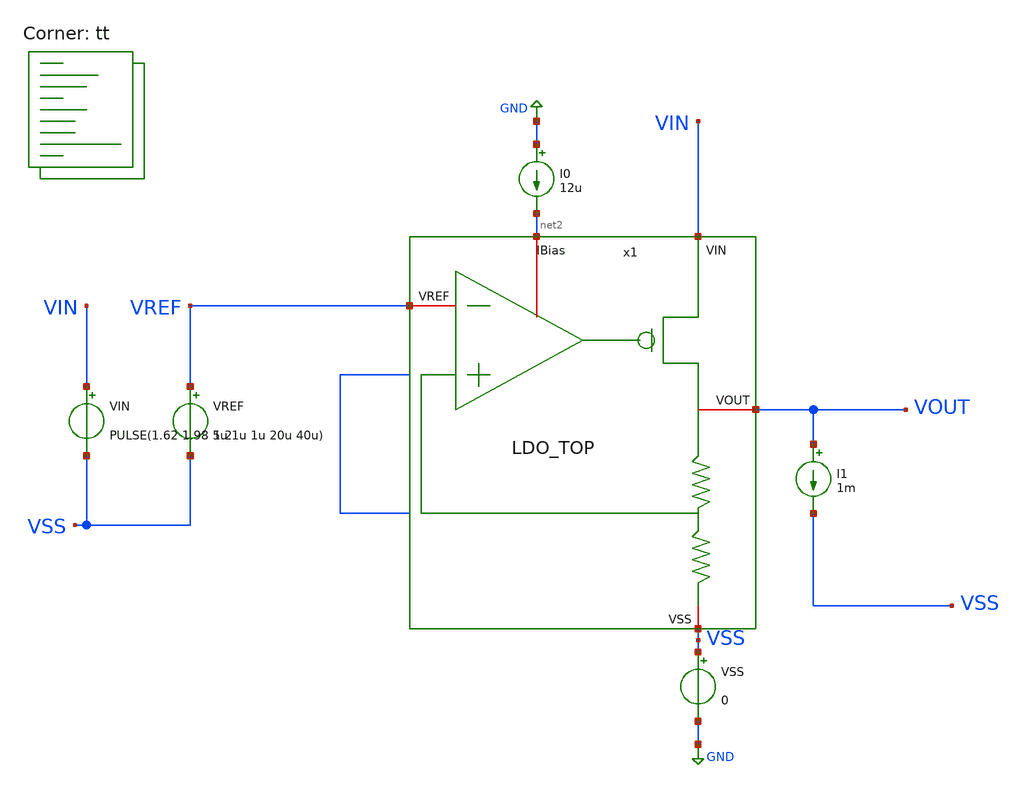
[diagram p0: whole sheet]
** sch_path: LDO_1p5V/tests/Line_tran.sch
**.subckt Line_tran
VSS VSS GND 0
VREF VREF VSS 1.2
VIN VIN VSS PULSE(1.62 1.98 5u 1u 1u 20u 40u)
I0 GND net2 12u
I1 VOUT VSS 1m
x1 VIN net2 VREF VOUT VSS LDO_TOP
**** begin user architecture code


.options savecurrents
.save all
.save v(x1.vgate)

.control
set filetype=ascii

echo ==========================================
echo ===== LDO LINE TRANSIENT ANALYSIS =====
echo ==========================================

op

echo ===== OPERATING POINT =====
print v(VIN)
print v(VOUT)
print v(VREF)
print v(x1.vgate)

echo ===== TRANSIENT ANALYSIS =====

* Fuente VIN recomendada en el esquemático:
* VIN PULSE(1.62 1.98 5u 1u 1u 20u 40u)
*
* Carga fija recomendada:
* ILOAD1 DC 1m

tran 10n 100u

echo ==========================================
echo ===== LINE TRANSIENT MEASUREMENTS =====
echo ==========================================

* VOUT nominal = 1.5 V
* Settling band = +/-1%
* Lower band = 1.485 V
* Upper band = 1.515 V

****************************************************
* GLOBAL MIN/MAX
****************************************************

meas tran vout_min_all min v(VOUT)
meas tran vout_max_all max v(VOUT)

let global_undershoot_mv = (1.5 - vout_min_all)*1000
let global_overshoot_mv  = (vout_max_all - 1.5)*1000

****************************************************
* STEP 1: VIN RISE 1.62V -> 1.98V
* Starts at 5us, ends at 6us
****************************************************

meas tran vout_max_step1 max v(VOUT) from=5u to=26u
meas tran vout_min_step1 min v(VOUT) from=5u to=26u

let overshoot_step1_mv  = (vout_max_step1 - 1.5)*1000
let undershoot_step1_mv = (1.5 - vout_min_step1)*1000

* Settling after VIN rise:
* If VOUT goes above nominal, measure when it returns below upper band.
meas tran t_settle_step1_abs when v(VOUT)=1.515 fall=1 from=5u to=26u

let t_settle_step1 = t_settle_step1_abs - 5u
let t_settle_step1_us = t_settle_step1*1e6

****************************************************
* STEP 2: VIN FALL 1.98V -> 1.62V
* Starts at 26us, ends at 27us
****************************************************

meas tran vout_max_step2 max v(VOUT) from=26u to=45u
meas tran vout_min_step2 min v(VOUT) from=26u to=45u

let overshoot_step2_mv  = (vout_max_step2 - 1.5)*1000
let undershoot_step2_mv = (1.5 - vout_min_step2)*1000

* Settling after VIN fall:
* If VOUT goes below nominal, measure when it returns above lower band.
meas tran t_settle_step2_abs when v(VOUT)=1.485 rise=1 from=26u to=45u

let t_settle_step2 = t_settle_step2_abs - 26u
let t_settle_step2_us = t_settle_step2*1e6

****************************************************
* STEP 3: SECOND VIN RISE 1.62V -> 1.98V
* Starts at 45us, ends at 46us
****************************************************

meas tran vout_max_step3 max v(VOUT) from=45u to=66u
meas tran vout_min_step3 min v(VOUT) from=45u to=66u

let overshoot_step3_mv  = (vout_max_step3 - 1.5)*1000
let undershoot_step3_mv = (1.5 - vout_min_step3)*1000

meas tran t_settle_step3_abs when v(VOUT)=1.515 fall=1 from=45u to=66u

let t_settle_step3 = t_settle_step3_abs - 45u
let t_settle_step3_us = t_settle_step3*1e6

****************************************************
* STEP 4: SECOND VIN FALL 1.98V -> 1.62V
* Starts at 66us, ends at 67us
****************************************************

meas tran vout_max_step4 max v(VOUT) from=66u to=85u
meas tran vout_min_step4 min v(VOUT) from=66u to=85u

let overshoot_step4_mv  = (vout_max_step4 - 1.5)*1000
let undershoot_step4_mv = (1.5 - vout_min_step4)*1000

meas tran t_settle_step4_abs when v(VOUT)=1.485 rise=1 from=66u to=85u

let t_settle_step4 = t_settle_step4_abs - 66u
let t_settle_step4_us = t_settle_step4*1e6

****************************************************
* RESULTS
****************************************************

echo ===== GLOBAL RESULTS =====
print vout_min_all
print vout_max_all
print global_undershoot_mv
print global_overshoot_mv

echo ===== STEP 1: VIN 1.62V -> 1.98V =====
print vout_max_step1
print vout_min_step1
print overshoot_step1_mv
print undershoot_step1_mv
print t_settle_step1_us

echo ===== STEP 2: VIN 1.98V -> 1.62V =====
print vout_max_step2
print vout_min_step2
print overshoot_step2_mv
print undershoot_step2_mv
print t_settle_step2_us

echo ===== STEP 3: VIN 1.62V -> 1.98V =====
print vout_max_step3
print vout_min_step3
print overshoot_step3_mv
print undershoot_step3_mv
print t_settle_step3_us

echo ===== STEP 4: VIN 1.98V -> 1.62V =====
print vout_max_step4
print vout_min_step4
print overshoot_step4_mv
print undershoot_step4_mv
print t_settle_step4_us

****************************************************
* PLOTS
****************************************************

echo ===== PLOTS =====

plot v(VIN)
plot v(VOUT)
plot v(x1.vgate)
plot v(VOUT) v(VIN)
plot v(VOUT) v(x1.vgate)

.endc


.lib $::SKYWATER_MODELS/sky130.lib.spice tt
**** end user architecture code
**.ends

* expanding   symbol:  /foss/designs/Curso_Semiconductores/LDO_1p5V/schematics/LDO_TOP.sym # of
*+ pins=5
** sym_path: LDO/LDO_TOP.sym
** sch_path: LDO/LDO_TOP.sch
.subckt LDO_TOP VIN IBias VREF VOUT VSS
*.iopin VIN
*.iopin VREF
*.iopin IBias
*.iopin VOUT
*.iopin VSS
x1 VIN IBias VREF VOUT net1 net1 VSS LDO
.ends


* expanding   symbol:  /foss/designs/Curso_Semiconductores/LDO/LDO.sym # of pins=7
** sym_path: LDO/LDO.sym
** sch_path: LDO/LDO.sch
.subckt LDO VIN IBias VREF VOUT VFB1 VFB2 VSS
*.iopin VIN
*.iopin VREF
*.iopin VFB1
*.iopin VSS
*.iopin VFB2
*.iopin VOUT
*.iopin IBias
XM7 VOUT Vgate VIN VIN sky130_fd_pr__pfet_01v8 L=0.15 W=6 nf=1 ad='int((1 + 1)/2) * 6 / 1 * 0.29' as='int((1 + 2)/2) * 6 / 1 * 0.29'
+ pd='2*int((1 + 1)/2) * (6 / 1 + 0.29)' ps='2*int((1 + 2)/2) * (6 / 1 + 0.29)' nrd='0.29 / 6 ' nrs='0.29 / 6 '
+ sa=0 sb=0 sd=0 mult=50 m=50
XC3 Vgate VOUT sky130_fd_pr__model__cap_mim W=10 L=10 MF=1 m=1
x1 VIN Vgate VREF VFB1 IBias VSS OTA_5T
x2 VOUT VFB2 VSS RES_FB
.ends


* expanding   symbol:  /foss/designs/Curso_Semiconductores/OTA_5T/OTA_5T.sym # of pins=6
** sym_path: /foss/designs/Curso_Semiconductores/OTA_5T/OTA_5T.sym
** sch_path: /foss/designs/Curso_Semiconductores/OTA_5T/OTA_5T.sch
.subckt OTA_5T VIN VOUT_AMP VINN VINP IB VSS
*.iopin VIN
*.iopin VSS
*.iopin VOUT_AMP
*.iopin IB
*.iopin VINN
*.iopin VINP
XM1 IB IB VSS VSS sky130_fd_pr__nfet_01v8 L=1 W=2.5 nf=1 ad='int((1 + 1)/2) * 2.5 / 1 * 0.29' as='int((1 + 2)/2) * 2.5 / 1 * 0.29'
+ pd='2*int((1 + 1)/2) * (2.5 / 1 + 0.29)' ps='2*int((1 + 2)/2) * (2.5 / 1 + 0.29)' nrd='0.29 / 2.5 ' nrs='0.29 / 2.5 '
+ sa=0 sb=0 sd=0 mult=4 m=4
XM2 tail IB VSS VSS sky130_fd_pr__nfet_01v8 L=1 W=2.5 nf=1 ad='int((1 + 1)/2) * 2.5 / 1 * 0.29' as='int((1 + 2)/2) * 2.5 / 1 * 0.29'
+ pd='2*int((1 + 1)/2) * (2.5 / 1 + 0.29)' ps='2*int((1 + 2)/2) * (2.5 / 1 + 0.29)' nrd='0.29 / 2.5 ' nrs='0.29 / 2.5 '
+ sa=0 sb=0 sd=0 mult=4 m=4
XM3 net1 VINP tail VSS sky130_fd_pr__nfet_01v8 L=1 W=3 nf=1 ad='int((1 + 1)/2) * 3 / 1 * 0.29' as='int((1 + 2)/2) * 3 / 1 * 0.29'
+ pd='2*int((1 + 1)/2) * (3 / 1 + 0.29)' ps='2*int((1 + 2)/2) * (3 / 1 + 0.29)' nrd='0.29 / 3 ' nrs='0.29 / 3 '
+ sa=0 sb=0 sd=0 mult=4 m=4
XM4 VOUT_AMP VINN tail VSS sky130_fd_pr__nfet_01v8 L=1 W=3 nf=1 ad='int((1 + 1)/2) * 3 / 1 * 0.29' as='int((1 + 2)/2) * 3 / 1 * 0.29'
+ pd='2*int((1 + 1)/2) * (3 / 1 + 0.29)' ps='2*int((1 + 2)/2) * (3 / 1 + 0.29)' nrd='0.29 / 3 ' nrs='0.29 / 3 '
+ sa=0 sb=0 sd=0 mult=4 m=4
XM5 VOUT_AMP net1 VIN VIN sky130_fd_pr__pfet_01v8 L=1 W=6 nf=1 ad='int((1 + 1)/2) * 6 / 1 * 0.29' as='int((1 + 2)/2) * 6 / 1 * 0.29'
+ pd='2*int((1 + 1)/2) * (6 / 1 + 0.29)' ps='2*int((1 + 2)/2) * (6 / 1 + 0.29)' nrd='0.29 / 6 ' nrs='0.29 / 6 '
+ sa=0 sb=0 sd=0 mult=4 m=4
XM6 net1 net1 VIN VIN sky130_fd_pr__pfet_01v8 L=1 W=6 nf=1 ad='int((1 + 1)/2) * 6 / 1 * 0.29' as='int((1 + 2)/2) * 6 / 1 * 0.29'
+ pd='2*int((1 + 1)/2) * (6 / 1 + 0.29)' ps='2*int((1 + 2)/2) * (6 / 1 + 0.29)' nrd='0.29 / 6 ' nrs='0.29 / 6 '
+ sa=0 sb=0 sd=0 mult=4 m=4
XD tail VSS tail VSS sky130_fd_pr__nfet_01v8 L=0.15 W=3 nf=1 ad='int((1 + 1)/2) * 3 / 1 * 0.29' as='int((1 + 2)/2) * 3 / 1 * 0.29'
+ pd='2*int((1 + 1)/2) * (3 / 1 + 0.29)' ps='2*int((1 + 2)/2) * (3 / 1 + 0.29)' nrd='0.29 / 3 ' nrs='0.29 / 3 '
+ sa=0 sb=0 sd=0 mult=4 m=4
XM7 VIN VIN VIN VIN sky130_fd_pr__pfet_01v8 L=0.15 W=6 nf=1 ad='int((1 + 1)/2) * 6 / 1 * 0.29' as='int((1 + 2)/2) * 6 / 1 * 0.29'
+ pd='2*int((1 + 1)/2) * (6 / 1 + 0.29)' ps='2*int((1 + 2)/2) * (6 / 1 + 0.29)' nrd='0.29 / 6 ' nrs='0.29 / 6 '
+ sa=0 sb=0 sd=0 mult=4 m=4
.ends


* expanding   symbol:  /foss/designs/Curso_Semiconductores/RES_FB/RES_FB.sym # of pins=3
** sym_path: RES_FB/RES_FB.sym
** sch_path: RES_FB/RES_FB.sch
.subckt RES_FB VOUT VFB VSS
*.iopin VOUT
*.iopin VFB
*.iopin VSS
XR11 net1 VOUT VSS sky130_fd_pr__res_xhigh_po_0p69 L=8.62 mult=1 m=1
XR1 VFB net1 VSS sky130_fd_pr__res_xhigh_po_0p69 L=8.62 mult=1 m=1
XR2 net8 VFB VSS sky130_fd_pr__res_xhigh_po_0p69 L=8.62 mult=1 m=1
XR3 net4 net8 VSS sky130_fd_pr__res_xhigh_po_0p69 L=8.62 mult=1 m=1
XR4 net2 net4 VSS sky130_fd_pr__res_xhigh_po_0p69 L=8.62 mult=1 m=1
XR5 net5 net2 VSS sky130_fd_pr__res_xhigh_po_0p69 L=8.62 mult=1 m=1
XR6 net3 net5 VSS sky130_fd_pr__res_xhigh_po_0p69 L=8.62 mult=1 m=1
XR7 net7 net3 VSS sky130_fd_pr__res_xhigh_po_0p69 L=8.62 mult=1 m=1
XR8 net6 net7 VSS sky130_fd_pr__res_xhigh_po_0p69 L=8.62 mult=1 m=1
XR9 VSS net6 VSS sky130_fd_pr__res_xhigh_po_0p69 L=8.62 mult=1 m=1
.ends

.GLOBAL GND
.end
